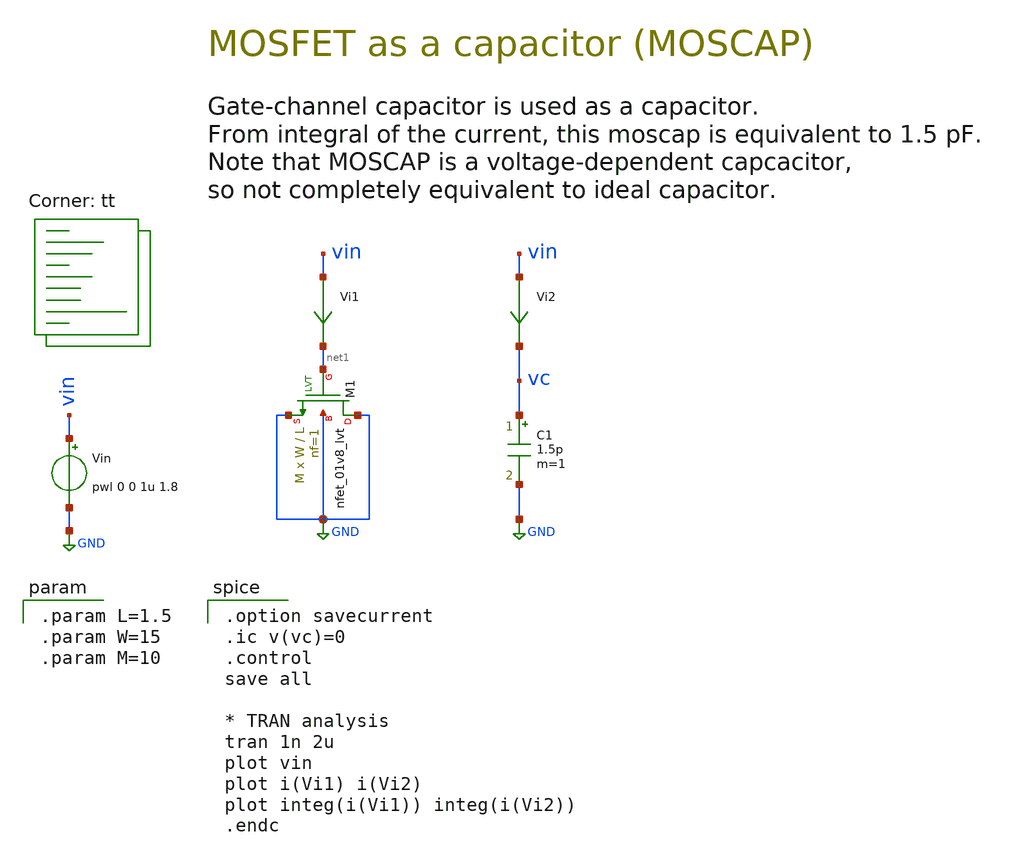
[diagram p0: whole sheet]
** sch_path: 00-d_moscap.sch
**.subckt 00-d_moscap
XM1 GND net1 GND GND sky130_fd_pr__nfet_01v8_lvt L=L W=W nf=1 ad='int((1 + 1)/2) * W / 1 * 0.29' as='int((1 + 2)/2) * W / 1 * 0.29'
+ pd='2*int((1 + 1)/2) * (W / 1 + 0.29)' ps='2*int((1 + 2)/2) * (W / 1 + 0.29)' nrd='0.29 / W ' nrs='0.29 / W '
+ sa=0 sb=0 sd=0 mult=M m=M
Vin vin GND pwl 0 0 1u 1.8
Vi1 vin net1 0
.save i(vi1)
C1 vc GND 1.5p m=1
Vi2 vin vc 0
.save i(vi2)
**** begin user architecture code
.lib $::SKYWATER_MODELS/sky130.lib.spice tt

.param L=1.5
.param W=15
.param M=10


.option savecurrent
.ic v(vc)=0
.control
save all

* TRAN analysis
tran 1n 2u
plot vin
plot i(Vi1) i(Vi2)
plot integ(i(Vi1)) integ(i(Vi2))
.endc

**** end user architecture code
**.ends
.GLOBAL GND
.end
